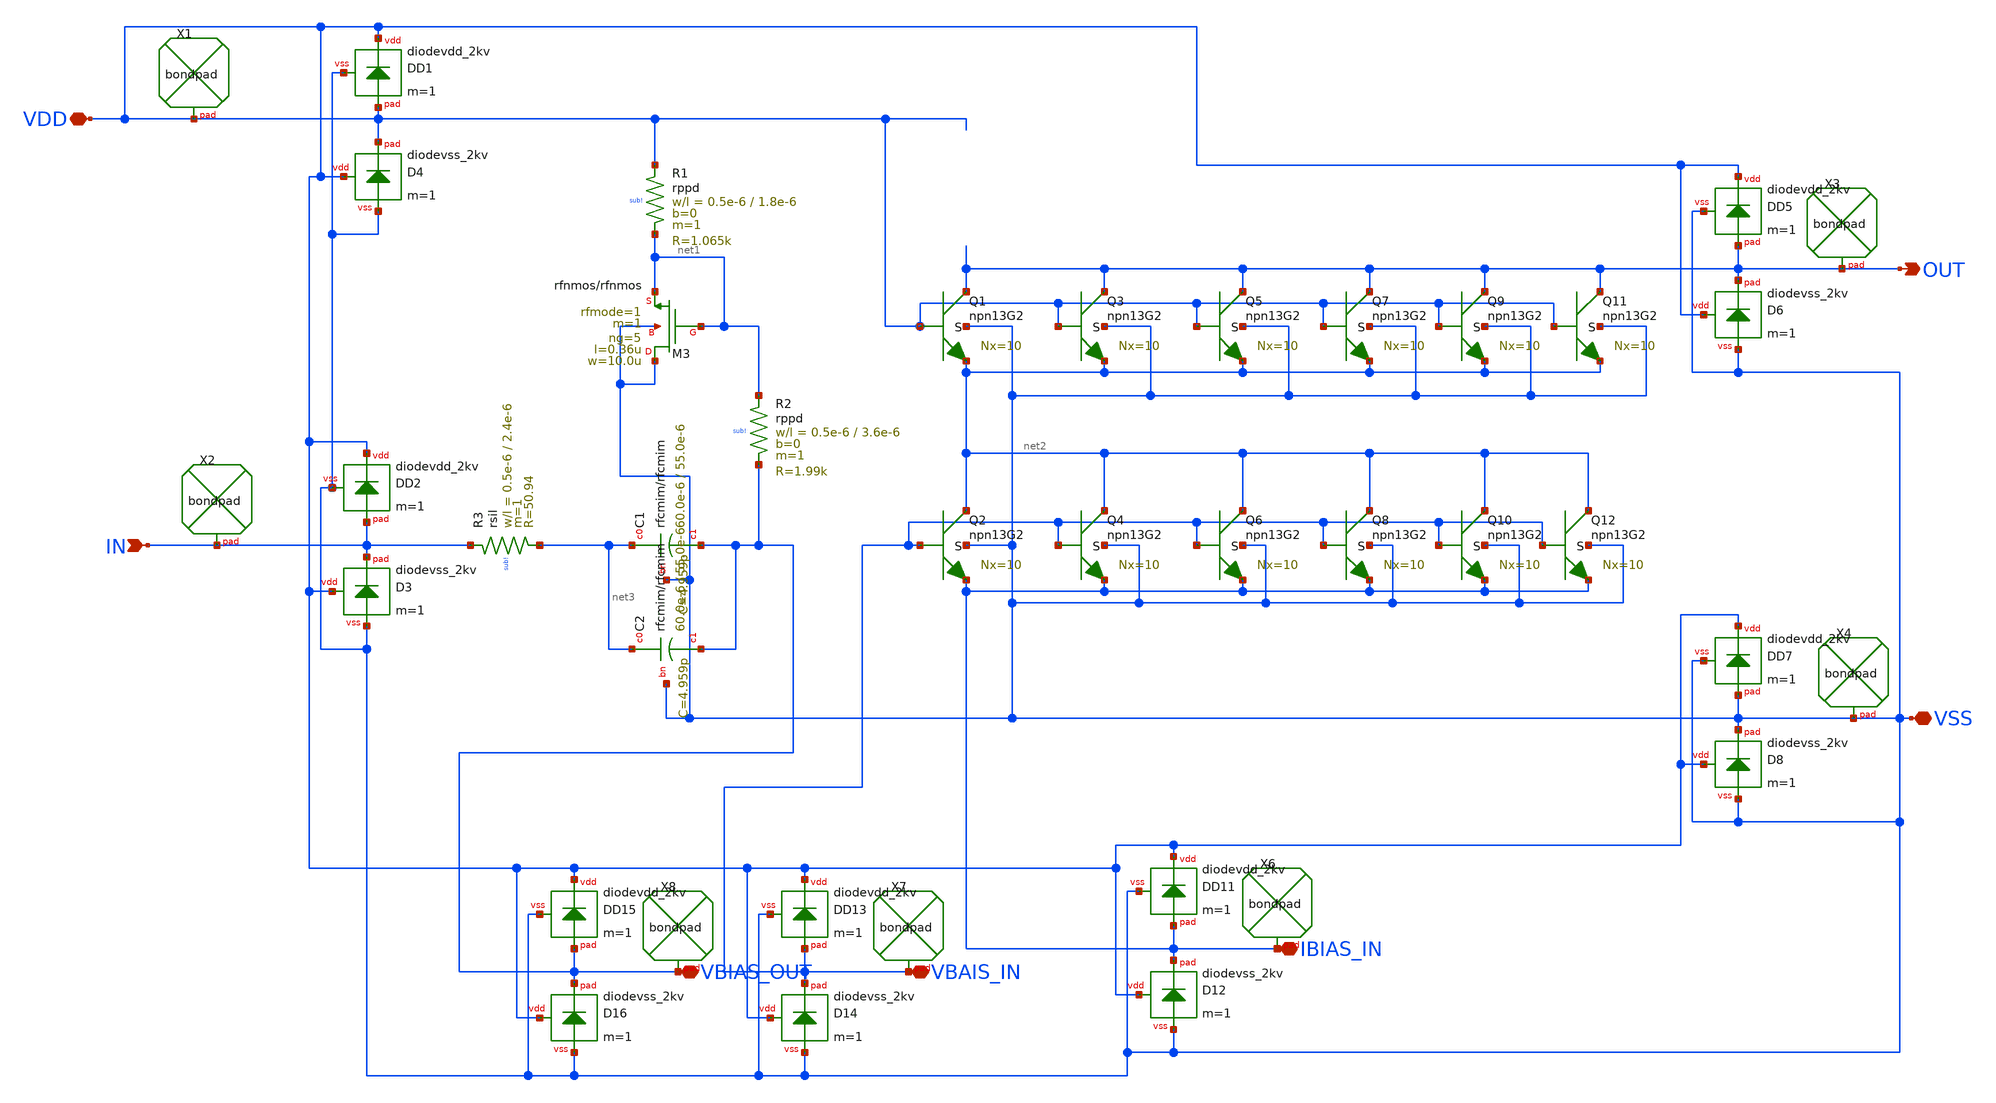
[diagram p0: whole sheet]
** sch_path: GPS_LNA/design_data/lvs/lna_npn_pad.sch
**.subckt lna_npn_pad VDD IN OUT VSS VBAIS_IN VBIAS_OUT IBIAS_IN
*.iopin VDD
*.ipin IN
*.opin OUT
*.iopin VSS
*.iopin VBAIS_IN
*.iopin VBIAS_OUT
*.iopin IBIAS_IN
XR2 net1 VBIAS_OUT sub! rppd w=0.5e-6 l=3.6e-6 m=1 b=0 mm_ok=1
XR1 VDD net1 sub! rppd w=0.5e-6 l=1.8e-6 m=1 b=0 mm_ok=1
XR3 IN net3 sub! rsil w=0.5e-6 l=2.4e-6 m=1 mm_ok=1
XC1 net3 VBIAS_OUT VSS rfcmim w=60.0e-6 l=55.0e-6 wfeed=5.0e-6 m=1 mm_ok=1
XC2 net3 VBIAS_OUT VSS rfcmim w=60.0e-6 l=55.0e-6 wfeed=5.0e-6 m=1 mm_ok=1
XM3 VSS net1 net1 VSS rfnmos w=10.0u l=0.36u ng=5 m=1 rfmode=1 mm_ok=1
XX1 VDD bondpad size=100u shape=0 padtype=0
XX3 OUT bondpad size=100u shape=0 padtype=0
XX4 VSS bondpad size=100u shape=0 padtype=0
XD1 VDD VDD VSS diodevdd_2kv m=1
XD4 VDD VDD VSS diodevss_2kv m=1
XX2 IN bondpad size=100u shape=0 padtype=0
XQ1 OUT VDD net2 VSS npn13G2 Nx=10 mm_ok=1
XQ2 net2 VBAIS_IN IBIAS_IN VSS npn13G2 Nx=10 mm_ok=1
XQ3 OUT VDD net2 VSS npn13G2 Nx=10 mm_ok=1
XQ4 net2 VBAIS_IN IBIAS_IN VSS npn13G2 Nx=10 mm_ok=1
XQ5 OUT VDD net2 VSS npn13G2 Nx=10 mm_ok=1
XQ6 net2 VBAIS_IN IBIAS_IN VSS npn13G2 Nx=10 mm_ok=1
XQ7 OUT VDD net2 VSS npn13G2 Nx=10 mm_ok=1
XQ8 net2 VBAIS_IN IBIAS_IN VSS npn13G2 Nx=10 mm_ok=1
XD2 VDD IN VSS diodevdd_2kv m=1
XD3 VDD IN VSS diodevss_2kv m=1
XD5 VDD OUT VSS diodevdd_2kv m=1
XD6 VDD OUT VSS diodevss_2kv m=1
XD7 VDD VSS VSS diodevdd_2kv m=1
XD8 VDD VSS VSS diodevss_2kv m=1
XQ9 OUT VDD net2 VSS npn13G2 Nx=10 mm_ok=1
XQ10 net2 VBAIS_IN IBIAS_IN VSS npn13G2 Nx=10 mm_ok=1
XQ11 OUT VDD net2 VSS npn13G2 Nx=10 mm_ok=1
XQ12 net2 VBAIS_IN IBIAS_IN VSS npn13G2 Nx=10 mm_ok=1
XX6 IBIAS_IN bondpad size=100u shape=0 padtype=0
XD11 VDD IBIAS_IN VSS diodevdd_2kv m=1
XD12 VDD IBIAS_IN VSS diodevss_2kv m=1
XX7 VBAIS_IN bondpad size=100u shape=0 padtype=0
XD13 VDD VBAIS_IN VSS diodevdd_2kv m=1
XD14 VDD VBAIS_IN VSS diodevss_2kv m=1
XX8 VBIAS_OUT bondpad size=100u shape=0 padtype=0
XD15 VDD VBIAS_OUT VSS diodevdd_2kv m=1
XD16 VDD VBIAS_OUT VSS diodevss_2kv m=1
**.ends
.end
